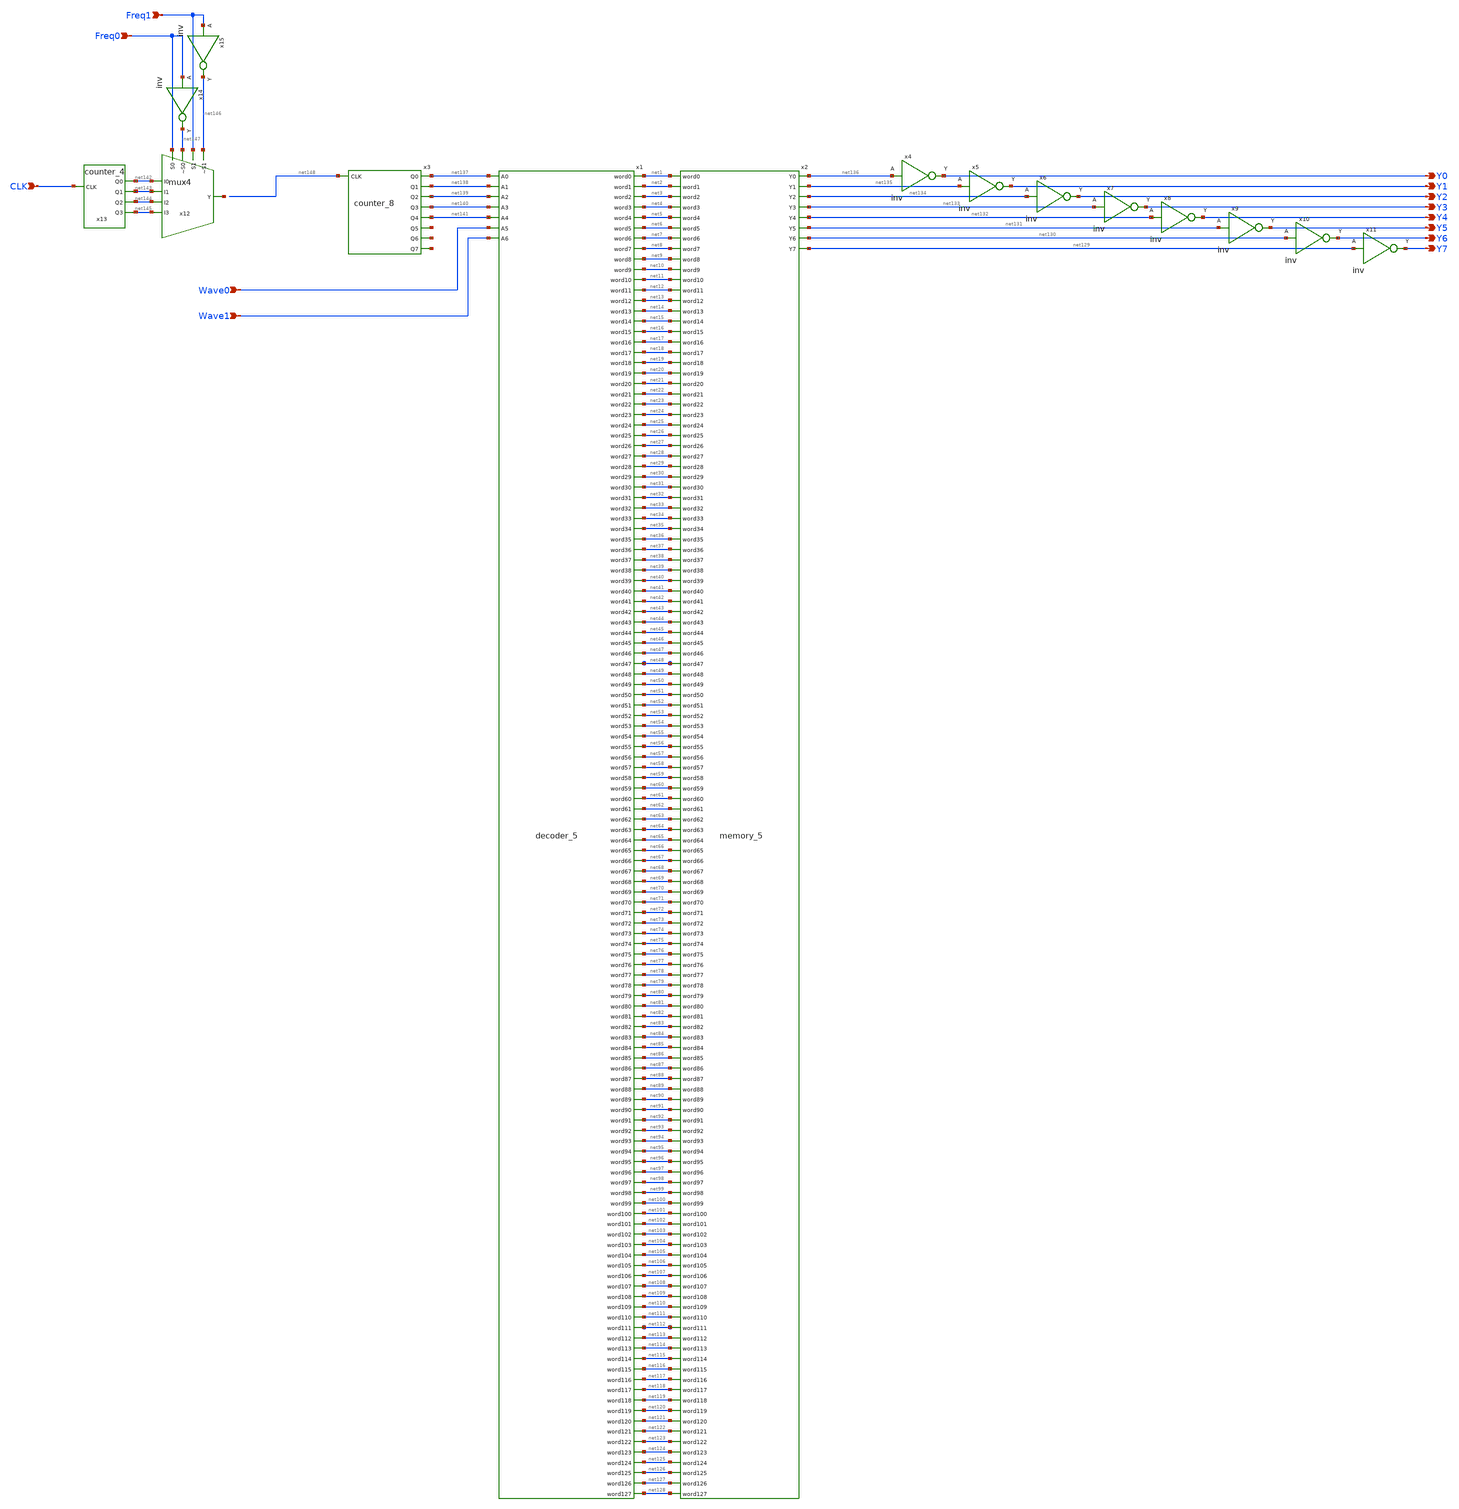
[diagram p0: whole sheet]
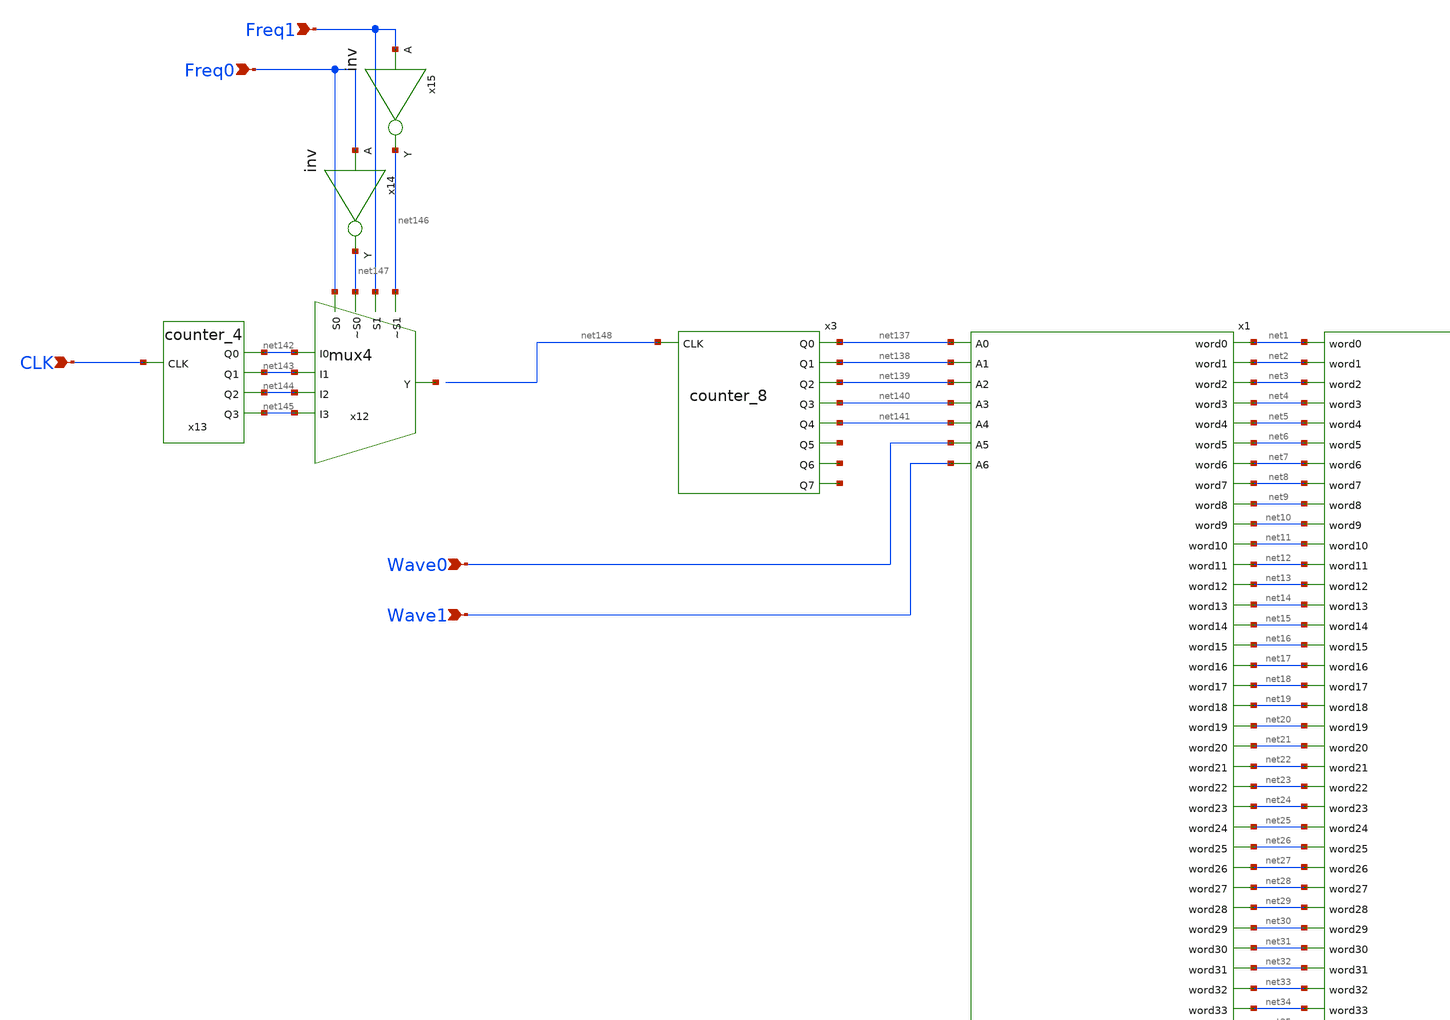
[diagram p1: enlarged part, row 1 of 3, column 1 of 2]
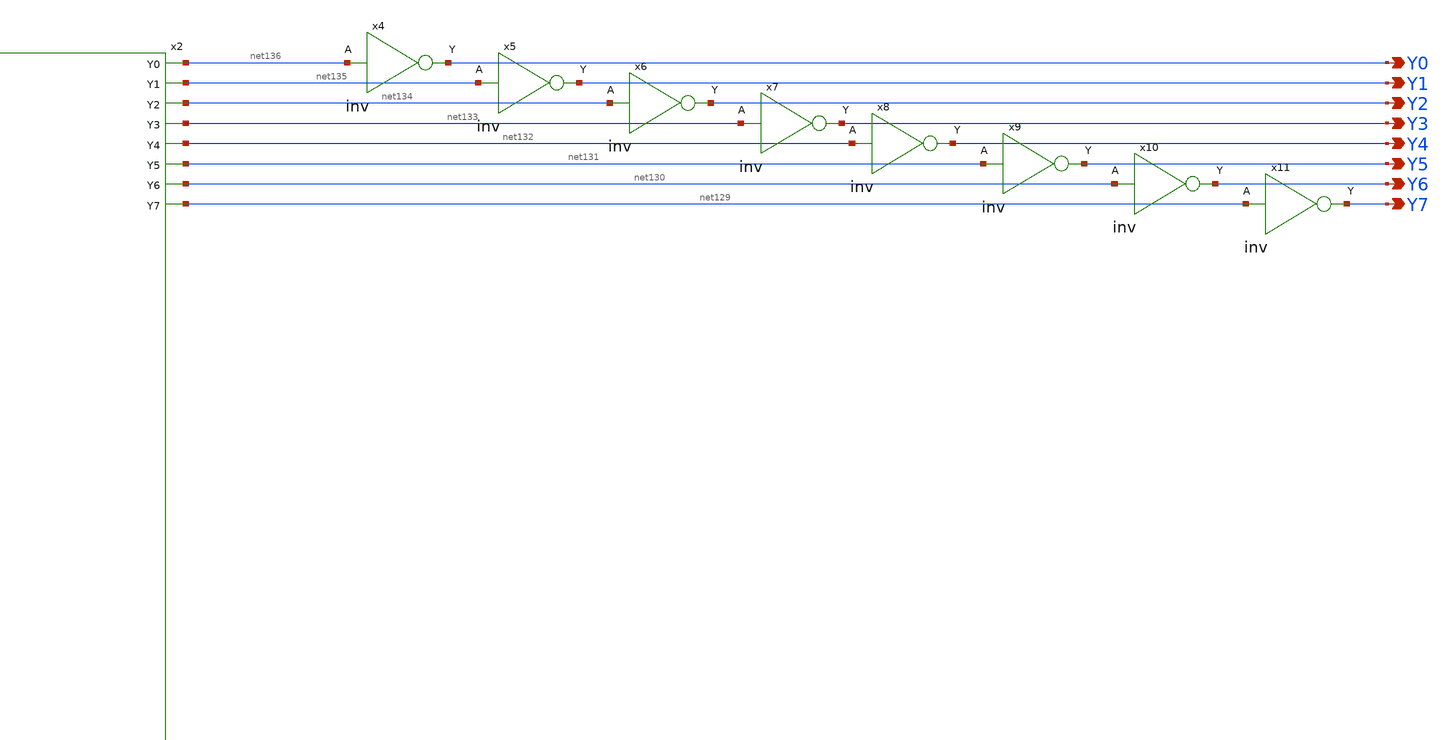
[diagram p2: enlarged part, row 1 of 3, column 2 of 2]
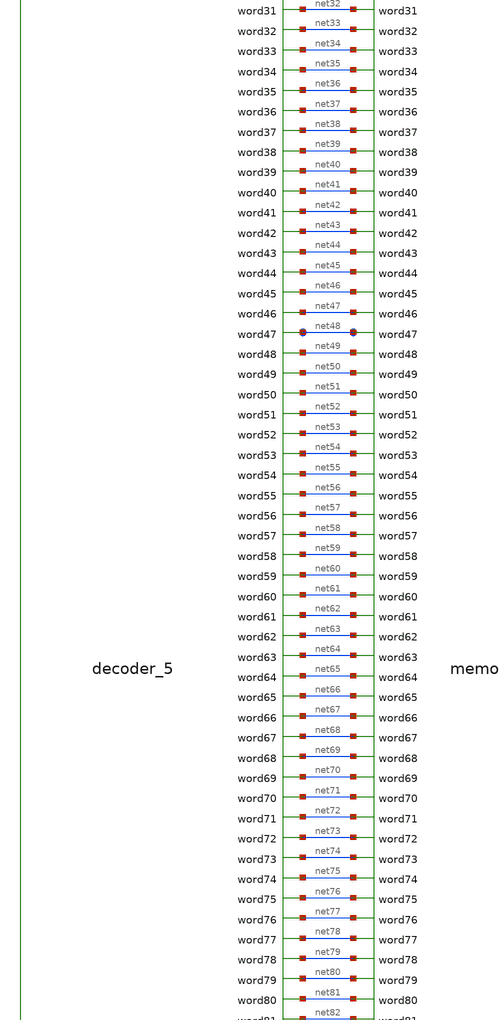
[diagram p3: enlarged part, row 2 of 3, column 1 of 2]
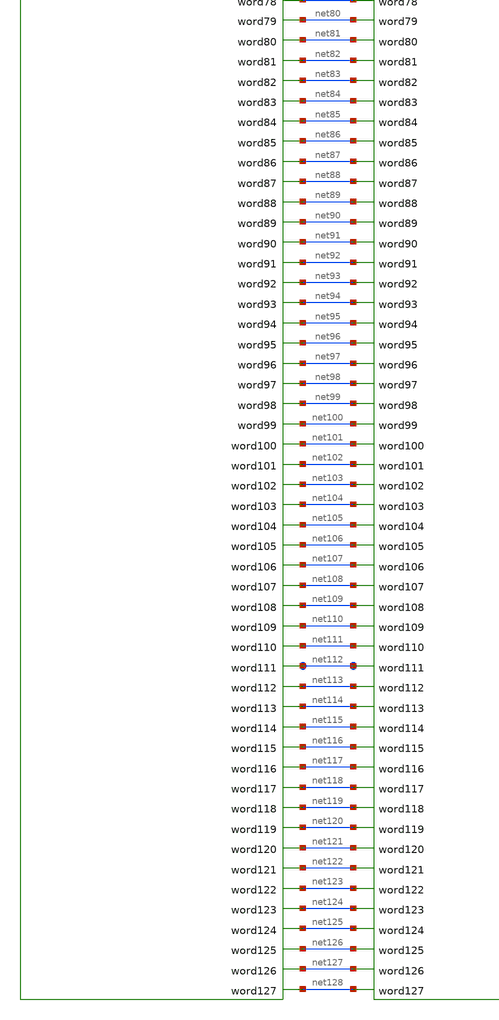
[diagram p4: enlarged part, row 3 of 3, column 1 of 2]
** sch_path: circuits/xschem/func_gen_freq.sch
**.subckt func_gen_freq CLK Freq0 Freq1 Y0 Y1 Y2 Y3 Y4 Y5 Y6 Y7 Wave0 Wave1
*.ipin CLK
*.ipin Freq0
*.ipin Freq1
*.opin Y0
*.opin Y1
*.opin Y2
*.opin Y3
*.opin Y4
*.opin Y5
*.opin Y6
*.opin Y7
*.ipin Wave0
*.ipin Wave1
x1 net138 Wave0 net140 net141 net139 Wave1 net137 net1 net2 net3 net4 net5 net6 net7 net8 net9 net10
+ net11 net12 net13 net14 net15 net16 net17 net18 net19 net20 net21 net22 net23 net24 net25 net26 net27
+ net28 net29 net30 net31 net32 net33 net34 net35 net36 net37 net38 net39 net40 net41 net42 net43 net44
+ net45 net46 net47 net48 net49 net50 net51 net52 net53 net54 net55 net56 net57 net58 net59 net60 net61
+ net62 net63 net64 net65 net66 net67 net68 net69 net70 net71 net72 net73 net74 net75 net76 net77 net78
+ net79 net80 net81 net82 net83 net84 net85 net86 net87 net88 net89 net90 net91 net92 net93 net94 net95
+ net96 net97 net98 net99 net100 net101 net102 net103 net104 net105 net106 net107 net108 net109 net110
+ net111 net112 net113 net114 net115 net116 net117 net118 net119 net120 net121 net122 net123 net124 net125
+ net126 net127 net128 decoder_5
x2 net1 net2 net3 net4 net5 net6 net7 net8 net9 net10 net11 net12 net13 net14 net15 net16 net17
+ net18 net19 net20 net21 net22 net23 net24 net25 net26 net27 net28 net29 net30 net31 net32 net33 net34
+ net35 net36 net37 net38 net39 net40 net41 net42 net43 net44 net45 net46 net47 net48 net49 net50 net51
+ net52 net53 net54 net55 net56 net57 net58 net59 net60 net61 net62 net63 net64 net65 net66 net67 net68
+ net69 net70 net71 net72 net73 net74 net75 net76 net77 net78 net79 net80 net81 net82 net83 net84 net85
+ net86 net87 net88 net89 net90 net91 net92 net93 net94 net95 net96 net97 net98 net99 net100 net101 net102
+ net103 net104 net105 net106 net107 net108 net109 net110 net111 net112 net113 net114 net115 net116 net117
+ net118 net119 net120 net121 net122 net123 net124 net125 net126 net127 net128 net136 net135 net134 net133
+ net132 net131 net130 net129 memory_5
x3 net137 net138 net139 net140 net141 net149 net150 net151 net148 counter_8
x4 Y0 net136 inv
x5 Y1 net135 inv
x6 Y2 net134 inv
x7 Y3 net133 inv
x8 Y4 net132 inv
x9 Y5 net131 inv
x10 Y6 net130 inv
x11 Y7 net129 inv
x12 Freq0 net147 Freq1 net146 net142 net143 net152 net144 net145 mux4
x13 net142 net143 net144 net145 CLK counter_4
x14 net147 Freq0 inv
x15 net146 Freq1 inv
**.ends
.end
